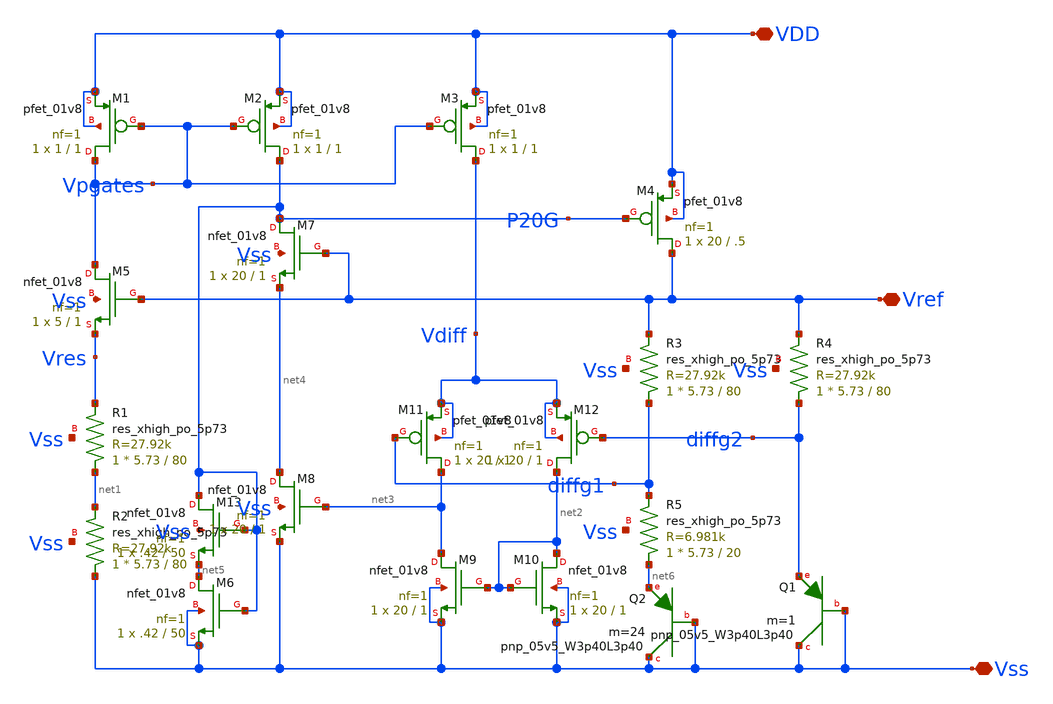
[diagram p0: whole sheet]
** sch_path: Project/xschem/bandgap.sch
**.subckt bandgap VDD Vss Vref
*.iopin VDD
*.iopin Vss
*.iopin Vref
XM7 P20G Vref net4 Vss sky130_fd_pr__nfet_01v8 L=1 W=20 nf=1 ad='int((nf+1)/2) * W/nf * 0.29' as='int((nf+2)/2) * W/nf * 0.29'
+ pd='2*int((nf+1)/2) * (W/nf + 0.29)' ps='2*int((nf+2)/2) * (W/nf + 0.29)' nrd='0.29 / W' nrs='0.29 / W'
+ sa=0 sb=0 sd=0 mult=1 m=1
XM1 Vpgates Vpgates VDD VDD sky130_fd_pr__pfet_01v8 L=1 W=1 nf=1 ad='int((nf+1)/2) * W/nf * 0.29' as='int((nf+2)/2) * W/nf * 0.29'
+ pd='2*int((nf+1)/2) * (W/nf + 0.29)' ps='2*int((nf+2)/2) * (W/nf + 0.29)' nrd='0.29 / W' nrs='0.29 / W'
+ sa=0 sb=0 sd=0 mult=1 m=1
XM2 P20G Vpgates VDD VDD sky130_fd_pr__pfet_01v8 L=1 W=1 nf=1 ad='int((nf+1)/2) * W/nf * 0.29' as='int((nf+2)/2) * W/nf * 0.29'
+ pd='2*int((nf+1)/2) * (W/nf + 0.29)' ps='2*int((nf+2)/2) * (W/nf + 0.29)' nrd='0.29 / W' nrs='0.29 / W'
+ sa=0 sb=0 sd=0 mult=1 m=1
XM3 Vdiff Vpgates VDD VDD sky130_fd_pr__pfet_01v8 L=1 W=1 nf=1 ad='int((nf+1)/2) * W/nf * 0.29' as='int((nf+2)/2) * W/nf * 0.29'
+ pd='2*int((nf+1)/2) * (W/nf + 0.29)' ps='2*int((nf+2)/2) * (W/nf + 0.29)' nrd='0.29 / W' nrs='0.29 / W'
+ sa=0 sb=0 sd=0 mult=1 m=1
XM4 Vref P20G VDD VDD sky130_fd_pr__pfet_01v8 L=.5 W=20 nf=1 ad='int((nf+1)/2) * W/nf * 0.29' as='int((nf+2)/2) * W/nf * 0.29'
+ pd='2*int((nf+1)/2) * (W/nf + 0.29)' ps='2*int((nf+2)/2) * (W/nf + 0.29)' nrd='0.29 / W' nrs='0.29 / W'
+ sa=0 sb=0 sd=0 mult=1 m=1
XM5 Vpgates Vref Vres Vss sky130_fd_pr__nfet_01v8 L=1 W=5 nf=1 ad='int((nf+1)/2) * W/nf * 0.29' as='int((nf+2)/2) * W/nf * 0.29'
+ pd='2*int((nf+1)/2) * (W/nf + 0.29)' ps='2*int((nf+2)/2) * (W/nf + 0.29)' nrd='0.29 / W' nrs='0.29 / W'
+ sa=0 sb=0 sd=0 mult=1 m=1
XR1 net1 Vres Vss sky130_fd_pr__res_xhigh_po_5p73 L=80 mult=1 m=1
XR2 Vss net1 Vss sky130_fd_pr__res_xhigh_po_5p73 L=80 mult=1 m=1
XM6 net5 P20G Vss Vss sky130_fd_pr__nfet_01v8 L=50 W=.42 nf=1 ad='int((nf+1)/2) * W/nf * 0.29' as='int((nf+2)/2) * W/nf * 0.29'
+ pd='2*int((nf+1)/2) * (W/nf + 0.29)' ps='2*int((nf+2)/2) * (W/nf + 0.29)' nrd='0.29 / W' nrs='0.29 / W'
+ sa=0 sb=0 sd=0 mult=1 m=1
XM8 net4 net3 Vss Vss sky130_fd_pr__nfet_01v8 L=1 W=20 nf=1 ad='int((nf+1)/2) * W/nf * 0.29' as='int((nf+2)/2) * W/nf * 0.29'
+ pd='2*int((nf+1)/2) * (W/nf + 0.29)' ps='2*int((nf+2)/2) * (W/nf + 0.29)' nrd='0.29 / W' nrs='0.29 / W'
+ sa=0 sb=0 sd=0 mult=1 m=1
XM9 net3 net2 Vss Vss sky130_fd_pr__nfet_01v8 L=1 W=20 nf=1 ad='int((nf+1)/2) * W/nf * 0.29' as='int((nf+2)/2) * W/nf * 0.29'
+ pd='2*int((nf+1)/2) * (W/nf + 0.29)' ps='2*int((nf+2)/2) * (W/nf + 0.29)' nrd='0.29 / W' nrs='0.29 / W'
+ sa=0 sb=0 sd=0 mult=1 m=1
XM10 net2 net2 Vss Vss sky130_fd_pr__nfet_01v8 L=1 W=20 nf=1 ad='int((nf+1)/2) * W/nf * 0.29' as='int((nf+2)/2) * W/nf * 0.29'
+ pd='2*int((nf+1)/2) * (W/nf + 0.29)' ps='2*int((nf+2)/2) * (W/nf + 0.29)' nrd='0.29 / W' nrs='0.29 / W'
+ sa=0 sb=0 sd=0 mult=1 m=1
XM11 net3 diffg1 Vdiff Vdiff sky130_fd_pr__pfet_01v8 L=1 W=20 nf=1 ad='int((nf+1)/2) * W/nf * 0.29' as='int((nf+2)/2) * W/nf * 0.29'
+ pd='2*int((nf+1)/2) * (W/nf + 0.29)' ps='2*int((nf+2)/2) * (W/nf + 0.29)' nrd='0.29 / W' nrs='0.29 / W'
+ sa=0 sb=0 sd=0 mult=1 m=1
XM12 net2 diffg2 Vdiff Vdiff sky130_fd_pr__pfet_01v8 L=1 W=20 nf=1 ad='int((nf+1)/2) * W/nf * 0.29' as='int((nf+2)/2) * W/nf * 0.29'
+ pd='2*int((nf+1)/2) * (W/nf + 0.29)' ps='2*int((nf+2)/2) * (W/nf + 0.29)' nrd='0.29 / W' nrs='0.29 / W'
+ sa=0 sb=0 sd=0 mult=1 m=1
XM13 P20G P20G net5 Vss sky130_fd_pr__nfet_01v8 L=50 W=.42 nf=1 ad='int((nf+1)/2) * W/nf * 0.29' as='int((nf+2)/2) * W/nf * 0.29'
+ pd='2*int((nf+1)/2) * (W/nf + 0.29)' ps='2*int((nf+2)/2) * (W/nf + 0.29)' nrd='0.29 / W' nrs='0.29 / W'
+ sa=0 sb=0 sd=0 mult=1 m=1
XR3 diffg1 Vref Vss sky130_fd_pr__res_xhigh_po_5p73 L=80 mult=1 m=1
XR4 diffg2 Vref Vss sky130_fd_pr__res_xhigh_po_5p73 L=80 mult=1 m=1
XR5 net6 diffg1 Vss sky130_fd_pr__res_xhigh_po_5p73 L=20 mult=1 m=1
XQ1 Vss Vss diffg2 sky130_fd_pr__pnp_05v5_W3p40L3p40 m=1
XQ2 Vss Vss net6 sky130_fd_pr__pnp_05v5_W3p40L3p40 m=24
**.ends
.end
